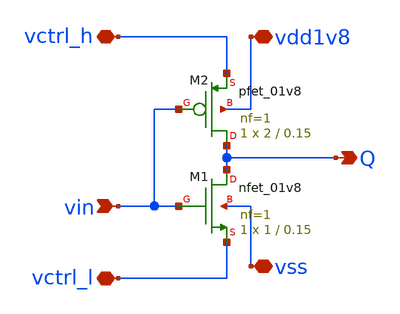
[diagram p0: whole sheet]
** sch_path: xschem/floating_comparator_0.sch
**.subckt floating_comparator_0 vdd1v8 vss Q vctrl_h vin vctrl_l
*.iopin vdd1v8
*.iopin vss
*.opin Q
*.iopin vctrl_h
*.ipin vin
*.iopin vctrl_l
XM1 Q vin vctrl_l vss sky130_fd_pr__nfet_01v8 L=0.15 W=1 nf=1 ad='int((nf+1)/2) * W/nf * 0.29' as='int((nf+2)/2) * W/nf * 0.29'
+ pd='2*int((nf+1)/2) * (W/nf + 0.29)' ps='2*int((nf+2)/2) * (W/nf + 0.29)' nrd='0.29 / W' nrs='0.29 / W'
+ sa=0 sb=0 sd=0 mult=1 m=1
XM2 Q vin vctrl_h vdd1v8 sky130_fd_pr__pfet_01v8 L=0.15 W=2 nf=1 ad='int((nf+1)/2) * W/nf * 0.29' as='int((nf+2)/2) * W/nf * 0.29'
+ pd='2*int((nf+1)/2) * (W/nf + 0.29)' ps='2*int((nf+2)/2) * (W/nf + 0.29)' nrd='0.29 / W' nrs='0.29 / W'
+ sa=0 sb=0 sd=0 mult=1 m=1
**.ends
.end
